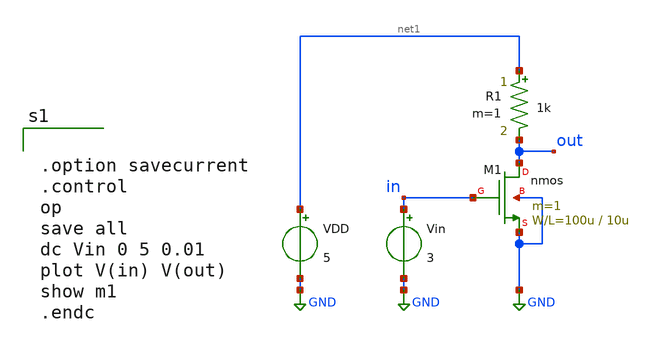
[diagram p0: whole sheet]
** sch_path: member_project/GroupWork/Team_masahiro/nfet_common_source.sch
**.subckt nfet_common_source
M1 out in GND GND nmos L=10u W=100u m=1
R1 net1 out 1k m=1
VDD net1 GND 5
Vin in GND 3
**** begin user architecture code
 .include $::LIB/mos.lib
.include $::LIB/passive.lib
.include $::LIB/diode.lib


.option savecurrent
.control
op
save all
dc Vin 0 5 0.01
plot V(in) V(out)
show m1
.endc


**** end user architecture code
**.ends
.GLOBAL GND
.end
